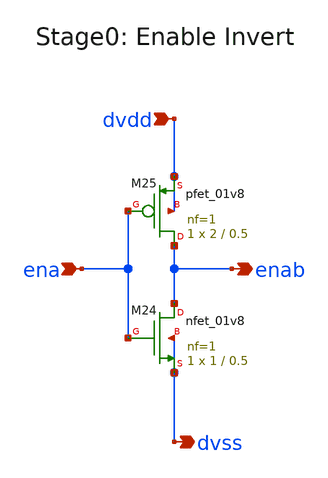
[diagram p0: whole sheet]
** sch_path: xschem/Stage0_ena_inv.sch
**.subckt Stage0_ena_inv ena dvdd dvss enab
*.ipin ena
*.ipin dvdd
*.opin dvss
*.opin enab
XM25 enab ena dvdd dvdd sky130_fd_pr__pfet_01v8 L=0.5 W=2 nf=1 ad='int((nf+1)/2) * W/nf * 0.29' as='int((nf+2)/2) * W/nf * 0.29'
+ pd='2*int((nf+1)/2) * (W/nf + 0.29)' ps='2*int((nf+2)/2) * (W/nf + 0.29)' nrd='0.29 / W' nrs='0.29 / W'
+ sa=0 sb=0 sd=0 mult=1 m=1
XM24 enab ena dvss dvss sky130_fd_pr__nfet_01v8 L=0.5 W=1 nf=1 ad='int((nf+1)/2) * W/nf * 0.29' as='int((nf+2)/2) * W/nf * 0.29'
+ pd='2*int((nf+1)/2) * (W/nf + 0.29)' ps='2*int((nf+2)/2) * (W/nf + 0.29)' nrd='0.29 / W' nrs='0.29 / W'
+ sa=0 sb=0 sd=0 mult=1 m=1
**.ends
.end
